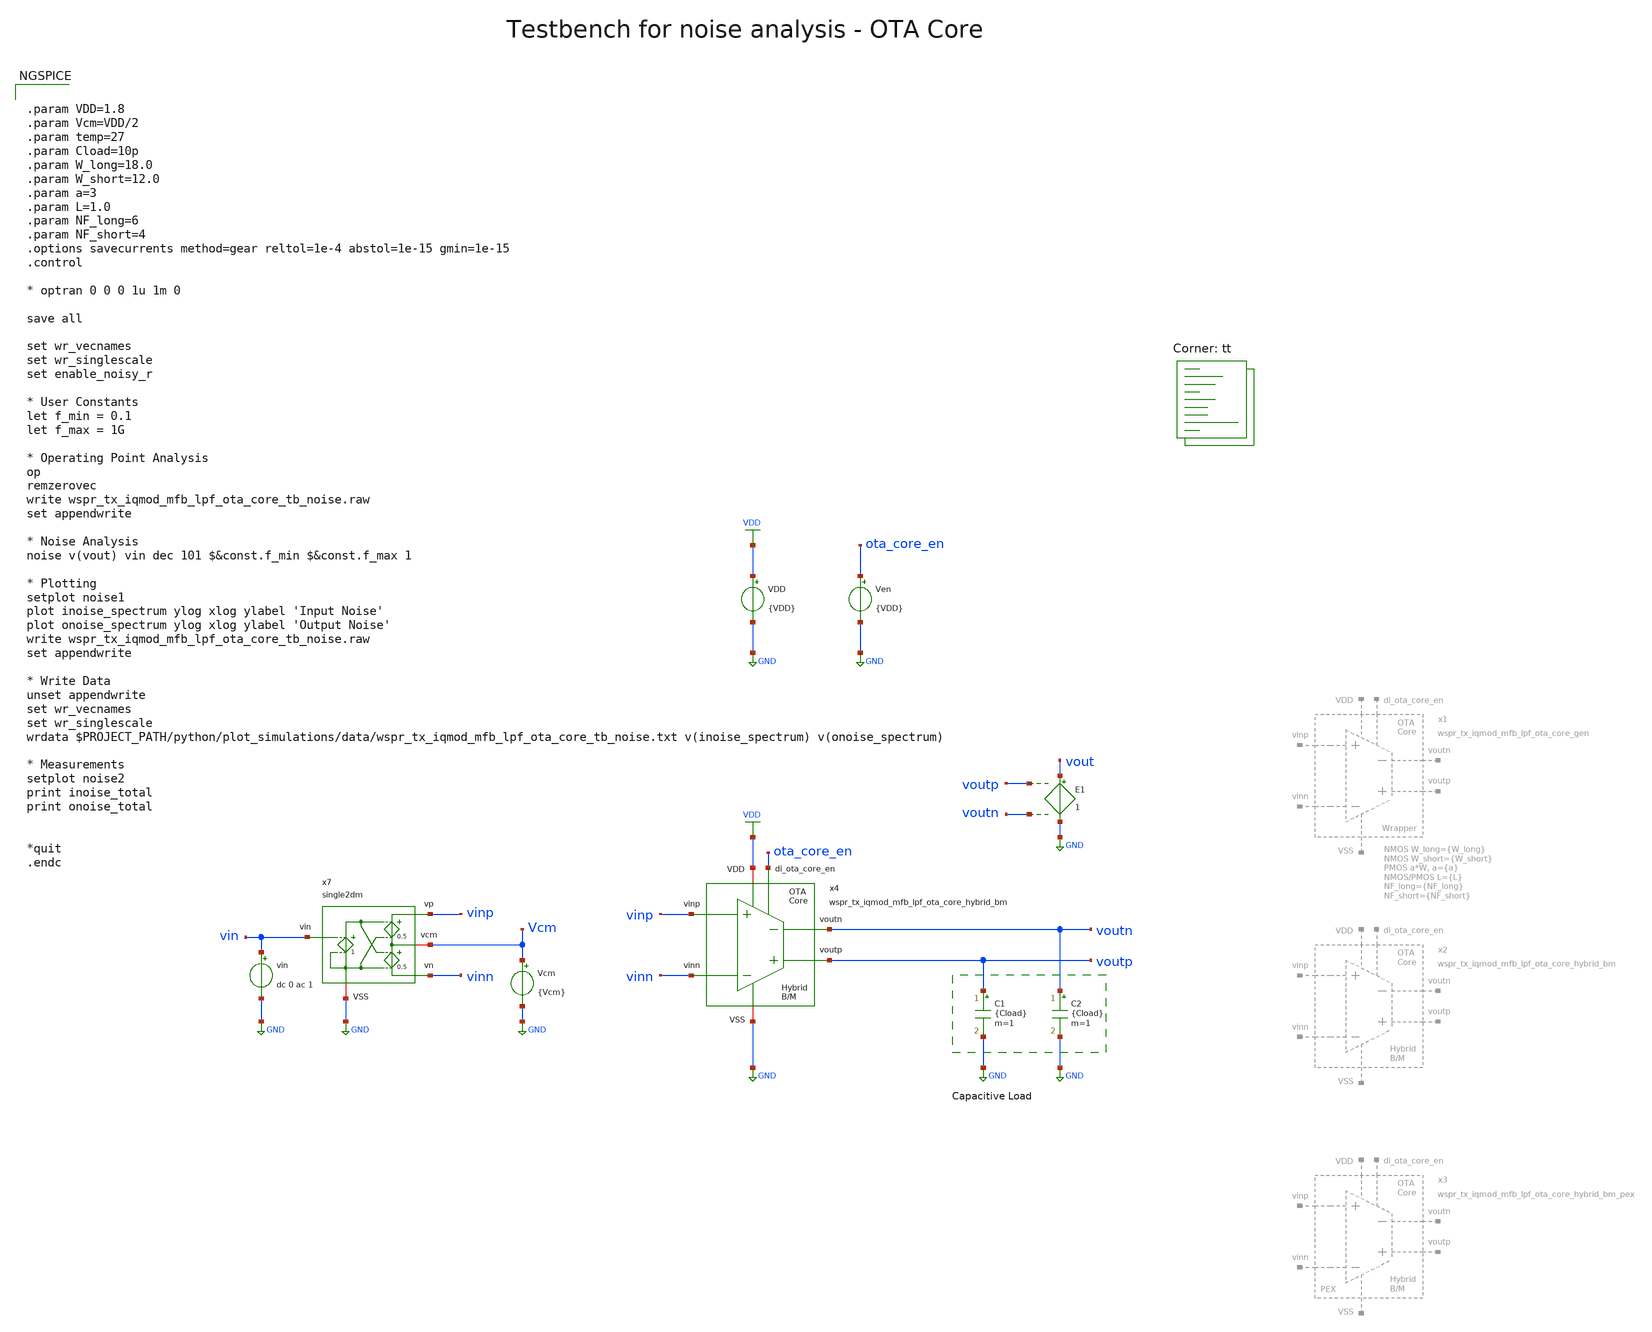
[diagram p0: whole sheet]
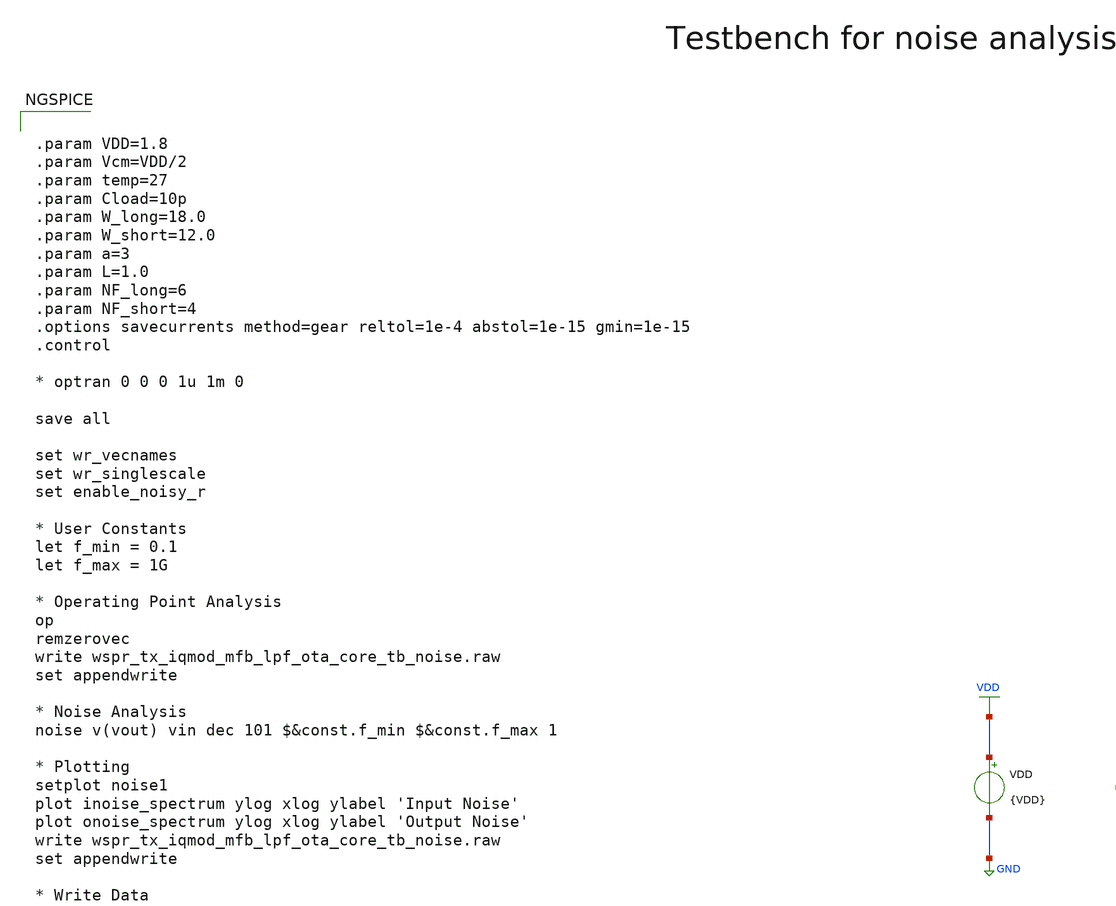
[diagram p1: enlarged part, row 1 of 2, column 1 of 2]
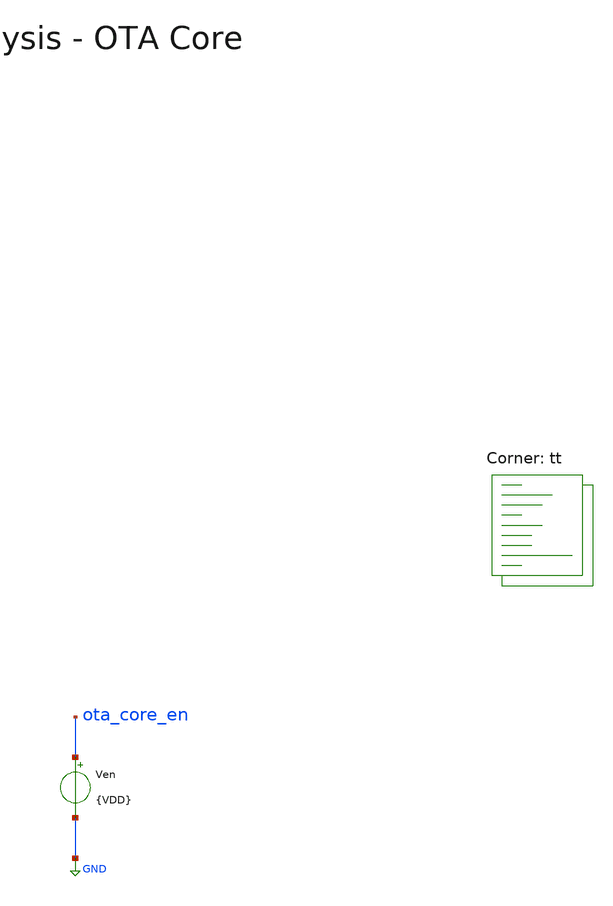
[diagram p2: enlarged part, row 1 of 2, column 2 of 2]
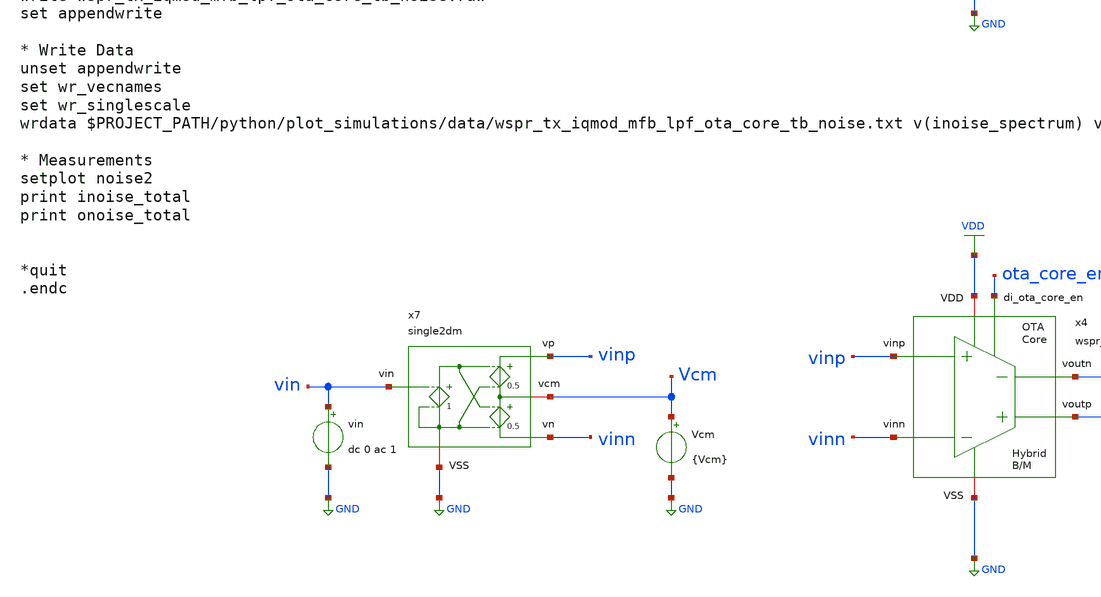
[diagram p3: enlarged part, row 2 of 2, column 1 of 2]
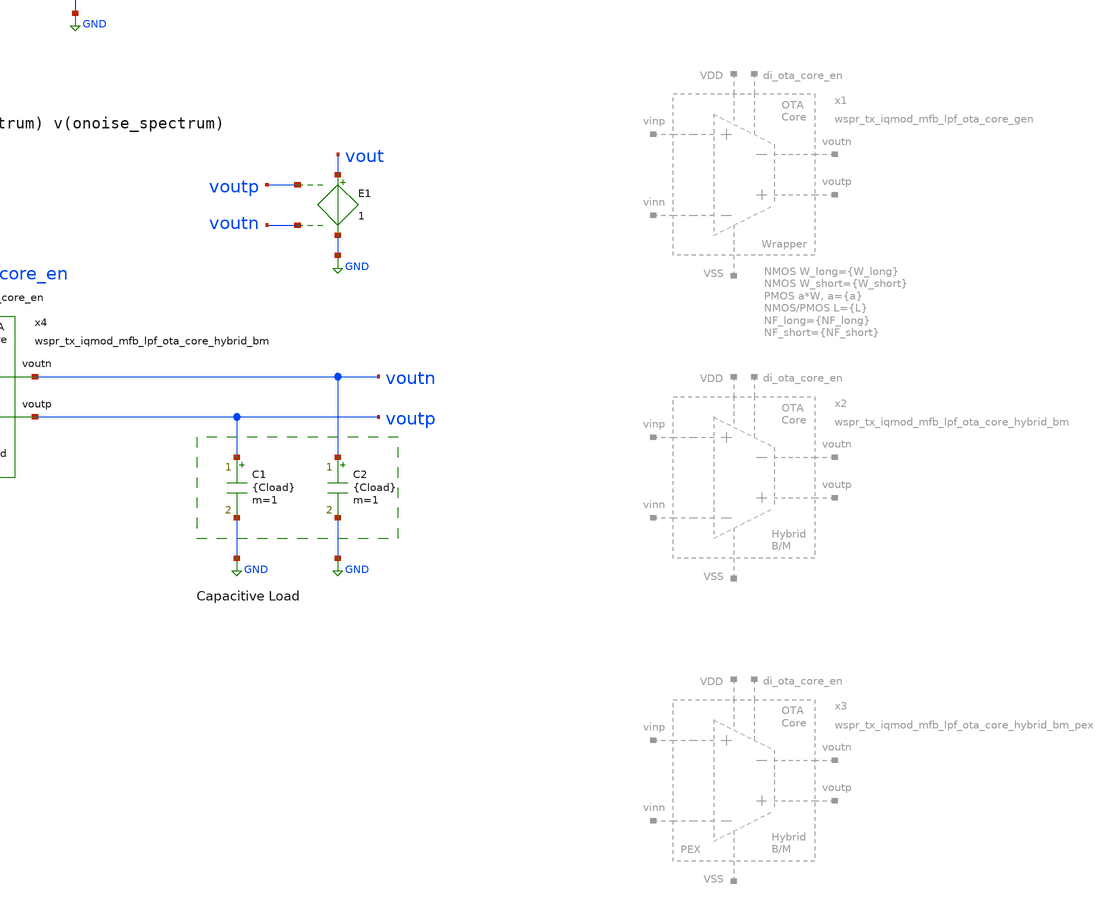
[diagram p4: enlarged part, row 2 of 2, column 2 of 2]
** sch_path: sky130/xschem/testbenches/wspr_tx_iqmod_mfb_lpf_ota_core_tb_noise.sch
**.subckt wspr_tx_iqmod_mfb_lpf_ota_core_tb_noise
VDD VDD GND {VDD}
C1 voutp GND {Cload} m=1
C2 voutn GND {Cload} m=1
Vcm Vcm GND {Vcm}
Ven ota_core_en GND {VDD}
E1 vout GND voutp voutn 1
vin vin GND dc 0 ac 1
x4 ota_core_en voutp voutn vinn vinp VDD GND wspr_tx_iqmod_mfb_lpf_ota_core_hybrid_bm
x7 vinp vin Vcm GND vinn single2dm
**** begin user architecture code


.param VDD=1.8
.param Vcm=VDD/2
.param temp=27
.param Cload=10p
.param W_long=18.0
.param W_short=12.0
.param a=3
.param L=1.0
.param NF_long=6
.param NF_short=4
.options savecurrents method=gear reltol=1e-4 abstol=1e-15 gmin=1e-15
.control

* optran 0 0 0 1u 1m 0

save all

set wr_vecnames
set wr_singlescale
set enable_noisy_r

* User Constants
let f_min = 0.1
let f_max = 1G

* Operating Point Analysis
op
remzerovec
write wspr_tx_iqmod_mfb_lpf_ota_core_tb_noise.raw
set appendwrite

* Noise Analysis
noise v(vout) vin dec 101 $&const.f_min $&const.f_max 1

* Plotting
setplot noise1
plot inoise_spectrum ylog xlog ylabel 'Input Noise'
plot onoise_spectrum ylog xlog ylabel 'Output Noise'
write wspr_tx_iqmod_mfb_lpf_ota_core_tb_noise.raw
set appendwrite

* Write Data
unset appendwrite
set wr_vecnames
set wr_singlescale
wrdata $PROJECT_PATH/python/plot_simulations/data/wspr_tx_iqmod_mfb_lpf_ota_core_tb_noise.txt
+ v(inoise_spectrum) v(onoise_spectrum)

* Measurements
setplot noise2
print inoise_total
print onoise_total


*quit
.endc


.lib $::SKYWATER_MODELS/sky130.lib.spice tt
**** end user architecture code
**.ends
.GLOBAL GND
.GLOBAL VDD
.end
